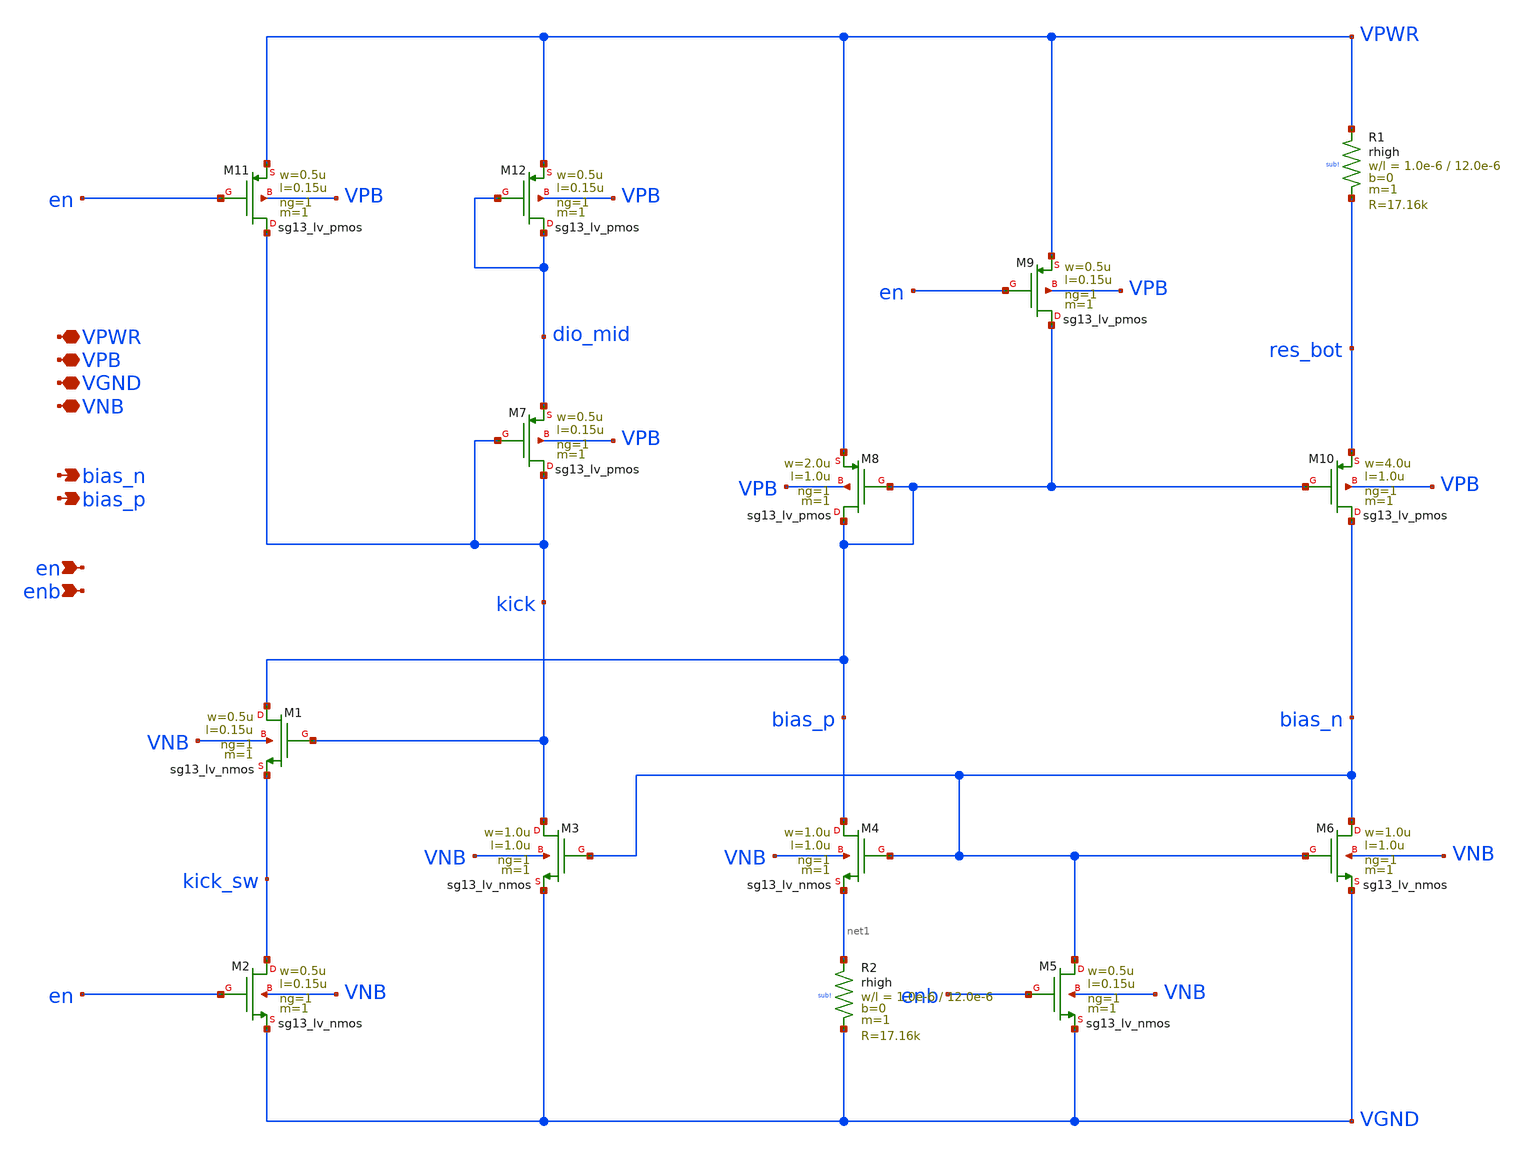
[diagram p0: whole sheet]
** sch_path: 30_MHz_Fractional_N_PLL/design_data/xschem/BIAS_GEN.sch
**.subckt BIAS_GEN en bias_n VNB VGND VPB VPWR enb bias_p
*.ipin en
*.opin bias_n
*.iopin VNB
*.iopin VGND
*.iopin VPB
*.iopin VPWR
*.ipin enb
*.opin bias_p
XM1 bias_p kick kick_sw VNB sg13_lv_nmos w=0.5u l=0.15u ng=1 m=1 mm_ok=1
XM2 kick_sw en VGND VNB sg13_lv_nmos w=0.5u l=0.15u ng=1 m=1 mm_ok=1
XM3 kick bias_n VGND VNB sg13_lv_nmos w=1.0u l=1.0u ng=1 m=1 mm_ok=1
XM4 bias_p bias_n net1 VNB sg13_lv_nmos w=1.0u l=1.0u ng=1 m=1 mm_ok=1
XM5 bias_n enb VGND VNB sg13_lv_nmos w=0.5u l=0.15u ng=1 m=1 mm_ok=1
XM6 bias_n bias_n VGND VNB sg13_lv_nmos w=1.0u l=1.0u ng=1 m=1 mm_ok=1
XM7 kick kick dio_mid VPB sg13_lv_pmos w=0.5u l=0.15u ng=1 m=1 mm_ok=1
XM8 bias_p bias_p VPWR VPB sg13_lv_pmos w=2.0u l=1.0u ng=1 m=1 mm_ok=1
XM9 bias_p en VPWR VPB sg13_lv_pmos w=0.5u l=0.15u ng=1 m=1 mm_ok=1
XM10 bias_n bias_p res_bot VPB sg13_lv_pmos w=4.0u l=1.0u ng=1 m=1 mm_ok=1
XM11 kick en VPWR VPB sg13_lv_pmos w=0.5u l=0.15u ng=1 m=1 mm_ok=1
XM12 dio_mid dio_mid VPWR VPB sg13_lv_pmos w=0.5u l=0.15u ng=1 m=1 mm_ok=1
XR1 VPWR res_bot sub! rhigh w=1.0e-6 l=12.0e-6 m=1 b=0 mm_ok=1
XR2 net1 VGND sub! rhigh w=1.0e-6 l=12.0e-6 m=1 b=0 mm_ok=1
**.ends
.end
